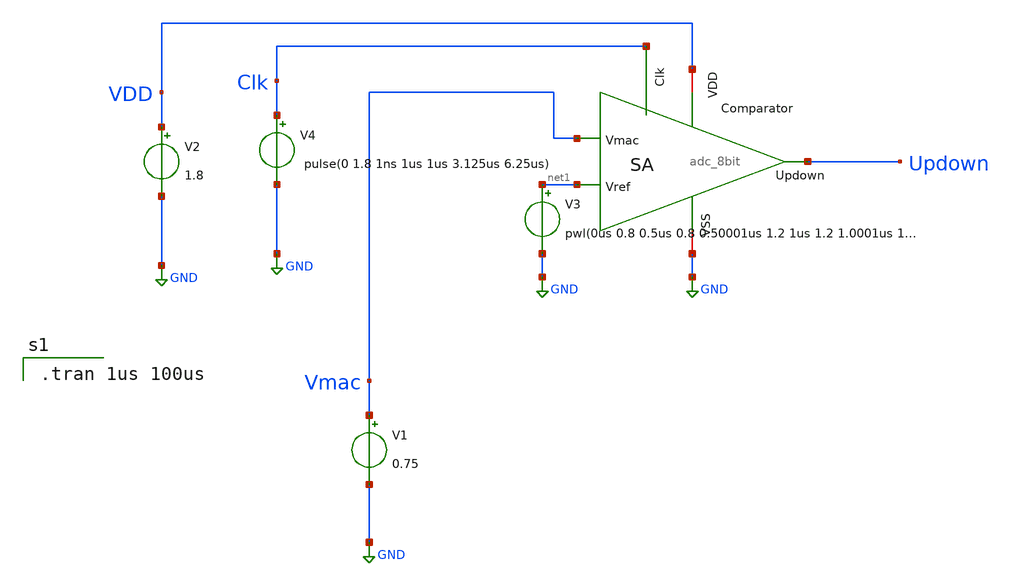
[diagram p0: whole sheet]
** sch_path: adc_comp/sim_adc_8bit.sch
**.subckt sim_adc_8bit
x1 GND VDD net1 Clk Vmac Updown adc_8bit
V2 VDD GND 1.8
V1 Vmac GND 0.75
V4 Clk GND pulse(0 1.8 1ns 1us 1us 3.125us 6.25us)
V3 net1 GND pwl(0us 0.8 0.5us 0.8 0.50001us 1.2 1us 1.2 1.0001us 1.4 2us 1.4 2.0001us 1.8 3us 1.8 )
**** begin user architecture code

.tran 1us 100us


** opencircuitdesign pdks install
.lib $::SKYWATER_MODELS/sky130.lib.spice tt
.include $::SKYWATER_STDCELLS/sky130_fd_sc_hd.spice

**** end user architecture code
**.ends

* expanding   symbol:  adc_8bit.sym # of pins=6
** sym_path: adc_comp/adc_8bit.sym
** sch_path: adc_comp/adc_8bit.sch
.subckt adc_8bit VSS VDD Vref Clk Vmac Updown
*.iopin VSS
*.iopin VDD
*.ipin Vref
*.ipin Vmac
*.ipin Clk
*.opin Updown
x1 Clk VSS VNB VPB VDD Clk_t sky130_fd_sc_hd__buf_1
x2 temp1 VSS VNB VPB VDD Updown sky130_fd_sc_hd__inv_1
x3 temp2 VSS VNB VPB VDD net4 sky130_fd_sc_hd__inv_1
XM1 net2 Clk_t VDD VDD sky130_fd_pr__pfet_01v8 L=0.35 W=1.075 nf=1 ad='int((nf+1)/2) * W/nf * 0.29' as='int((nf+2)/2) * W/nf * 0.29'
+ pd='2*int((nf+1)/2) * (W/nf + 0.29)' ps='2*int((nf+2)/2) * (W/nf + 0.29)' nrd='0.29 / W' nrs='0.29 / W'
+ sa=0 sb=0 sd=0 mult=1 m=1
XM2 temp2 Clk_t VDD VDD sky130_fd_pr__pfet_01v8 L=0.35 W=1.075 nf=1 ad='int((nf+1)/2) * W/nf * 0.29'
+ as='int((nf+2)/2) * W/nf * 0.29' pd='2*int((nf+1)/2) * (W/nf + 0.29)' ps='2*int((nf+2)/2) * (W/nf + 0.29)'
+ nrd='0.29 / W' nrs='0.29 / W' sa=0 sb=0 sd=0 mult=1 m=1
XM3 temp2 temp1 VDD VDD sky130_fd_pr__pfet_01v8 L=0.35 W=1.865 nf=1 ad='int((nf+1)/2) * W/nf * 0.29'
+ as='int((nf+2)/2) * W/nf * 0.29' pd='2*int((nf+1)/2) * (W/nf + 0.29)' ps='2*int((nf+2)/2) * (W/nf + 0.29)'
+ nrd='0.29 / W' nrs='0.29 / W' sa=0 sb=0 sd=0 mult=1 m=1
XM4 net1 Clk_t VDD VDD sky130_fd_pr__pfet_01v8 L=0.35 W=1.075 nf=1 ad='int((nf+1)/2) * W/nf * 0.29' as='int((nf+2)/2) * W/nf * 0.29'
+ pd='2*int((nf+1)/2) * (W/nf + 0.29)' ps='2*int((nf+2)/2) * (W/nf + 0.29)' nrd='0.29 / W' nrs='0.29 / W'
+ sa=0 sb=0 sd=0 mult=1 m=1
XM5 temp1 Clk_t VDD VDD sky130_fd_pr__pfet_01v8 L=0.35 W=1.075 nf=1 ad='int((nf+1)/2) * W/nf * 0.29'
+ as='int((nf+2)/2) * W/nf * 0.29' pd='2*int((nf+1)/2) * (W/nf + 0.29)' ps='2*int((nf+2)/2) * (W/nf + 0.29)'
+ nrd='0.29 / W' nrs='0.29 / W' sa=0 sb=0 sd=0 mult=1 m=1
XM6 temp1 temp2 VDD VDD sky130_fd_pr__pfet_01v8 L=0.35 W=1.865 nf=1 ad='int((nf+1)/2) * W/nf * 0.29'
+ as='int((nf+2)/2) * W/nf * 0.29' pd='2*int((nf+1)/2) * (W/nf + 0.29)' ps='2*int((nf+2)/2) * (W/nf + 0.29)'
+ nrd='0.29 / W' nrs='0.29 / W' sa=0 sb=0 sd=0 mult=1 m=1
XM7 temp2 temp1 net2 VSS sky130_fd_pr__nfet_01v8 L=0.15 W=0.6 nf=1 ad='int((nf+1)/2) * W/nf * 0.29' as='int((nf+2)/2) * W/nf * 0.29'
+ pd='2*int((nf+1)/2) * (W/nf + 0.29)' ps='2*int((nf+2)/2) * (W/nf + 0.29)' nrd='0.29 / W' nrs='0.29 / W'
+ sa=0 sb=0 sd=0 mult=1 m=1
XM8 temp1 temp2 net1 VSS sky130_fd_pr__nfet_01v8 L=0.15 W=0.6 nf=1 ad='int((nf+1)/2) * W/nf * 0.29' as='int((nf+2)/2) * W/nf * 0.29'
+ pd='2*int((nf+1)/2) * (W/nf + 0.29)' ps='2*int((nf+2)/2) * (W/nf + 0.29)' nrd='0.29 / W' nrs='0.29 / W'
+ sa=0 sb=0 sd=0 mult=1 m=1
XM9 net2 Vref net3 VSS sky130_fd_pr__nfet_01v8 L=0.15 W=0.6 nf=1 ad='int((nf+1)/2) * W/nf * 0.29' as='int((nf+2)/2) * W/nf * 0.29'
+ pd='2*int((nf+1)/2) * (W/nf + 0.29)' ps='2*int((nf+2)/2) * (W/nf + 0.29)' nrd='0.29 / W' nrs='0.29 / W'
+ sa=0 sb=0 sd=0 mult=1 m=1
XM10 net1 Vmac net3 VSS sky130_fd_pr__nfet_01v8 L=0.15 W=0.6 nf=1 ad='int((nf+1)/2) * W/nf * 0.29' as='int((nf+2)/2) * W/nf * 0.29'
+ pd='2*int((nf+1)/2) * (W/nf + 0.29)' ps='2*int((nf+2)/2) * (W/nf + 0.29)' nrd='0.29 / W' nrs='0.29 / W'
+ sa=0 sb=0 sd=0 mult=1 m=1
XM11 net3 Clk_t VSS VSS sky130_fd_pr__nfet_01v8 L=0.15 W=0.6 nf=1 ad='int((nf+1)/2) * W/nf * 0.29' as='int((nf+2)/2) * W/nf * 0.29'
+ pd='2*int((nf+1)/2) * (W/nf + 0.29)' ps='2*int((nf+2)/2) * (W/nf + 0.29)' nrd='0.29 / W' nrs='0.29 / W'
+ sa=0 sb=0 sd=0 mult=1 m=1
.ends

.GLOBAL GND
.end
